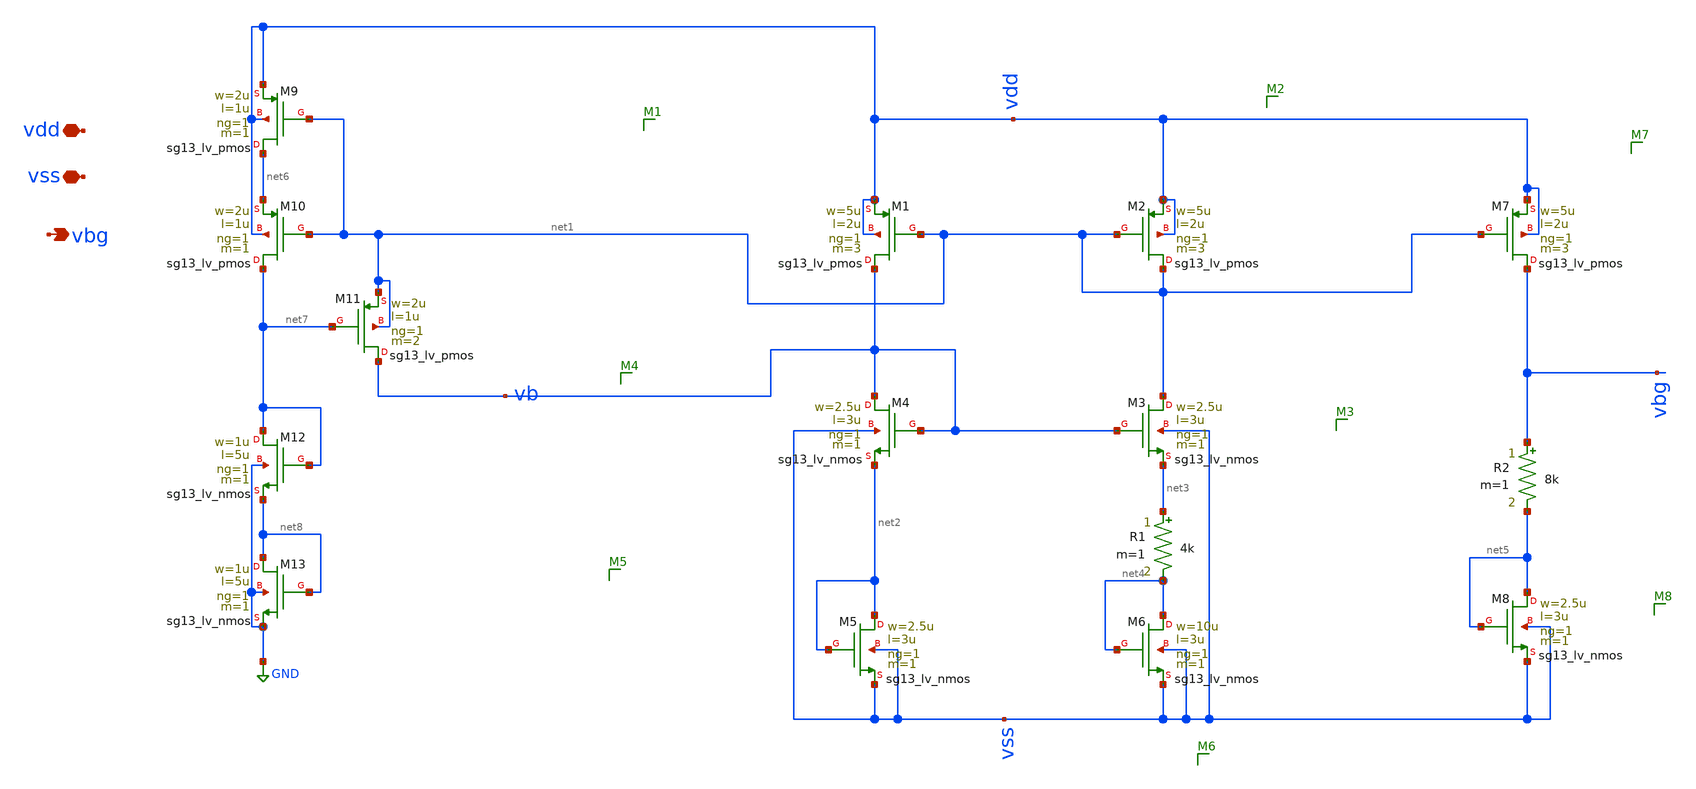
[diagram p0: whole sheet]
** sch_path: Schematics/bgr_cmos_circuit.sch
**.subckt bgr_cmos_circuit vdd vss vbg
*.iopin vdd
*.iopin vss
*.opin vbg
XM1 vb net1 vdd vdd sg13_lv_pmos w=5u l=2u ng=1 m=3 mm_ok=1
XM2 net1 net1 vdd vdd sg13_lv_pmos w=5u l=2u ng=1 m=3 mm_ok=1
XM3 net1 vb net3 vss sg13_lv_nmos w=2.5u l=3u ng=1 m=1 mm_ok=1
XM4 vb vb net2 vss sg13_lv_nmos w=2.5u l=3u ng=1 m=1 mm_ok=1
XM5 net2 net2 vss vss sg13_lv_nmos w=2.5u l=3u ng=1 m=1 mm_ok=1
R1 net3 net4 4k m=1
XM6 net4 net4 vss vss sg13_lv_nmos w=10u l=3u ng=1 m=1 mm_ok=1
XM7 vbg net1 vdd vdd sg13_lv_pmos w=5u l=2u ng=1 m=3 mm_ok=1
XM8 net5 net5 vss vss sg13_lv_nmos w=2.5u l=3u ng=1 m=1 mm_ok=1
R2 vbg net5 8k m=1
XM9 net6 net1 vdd vdd sg13_lv_pmos w=2u l=1u ng=1 m=1 mm_ok=1
XM10 net7 net1 net6 vdd sg13_lv_pmos w=2u l=1u ng=1 m=1 mm_ok=1
XM11 vb net7 net1 net1 sg13_lv_pmos w=2u l=1u ng=1 m=2 mm_ok=1
XM12 net7 net7 net8 GND sg13_lv_nmos w=1u l=5u ng=1 m=1 mm_ok=1
XM13 net8 net8 GND GND sg13_lv_nmos w=1u l=5u ng=1 m=1 mm_ok=1
**.ends
.GLOBAL GND
.end
